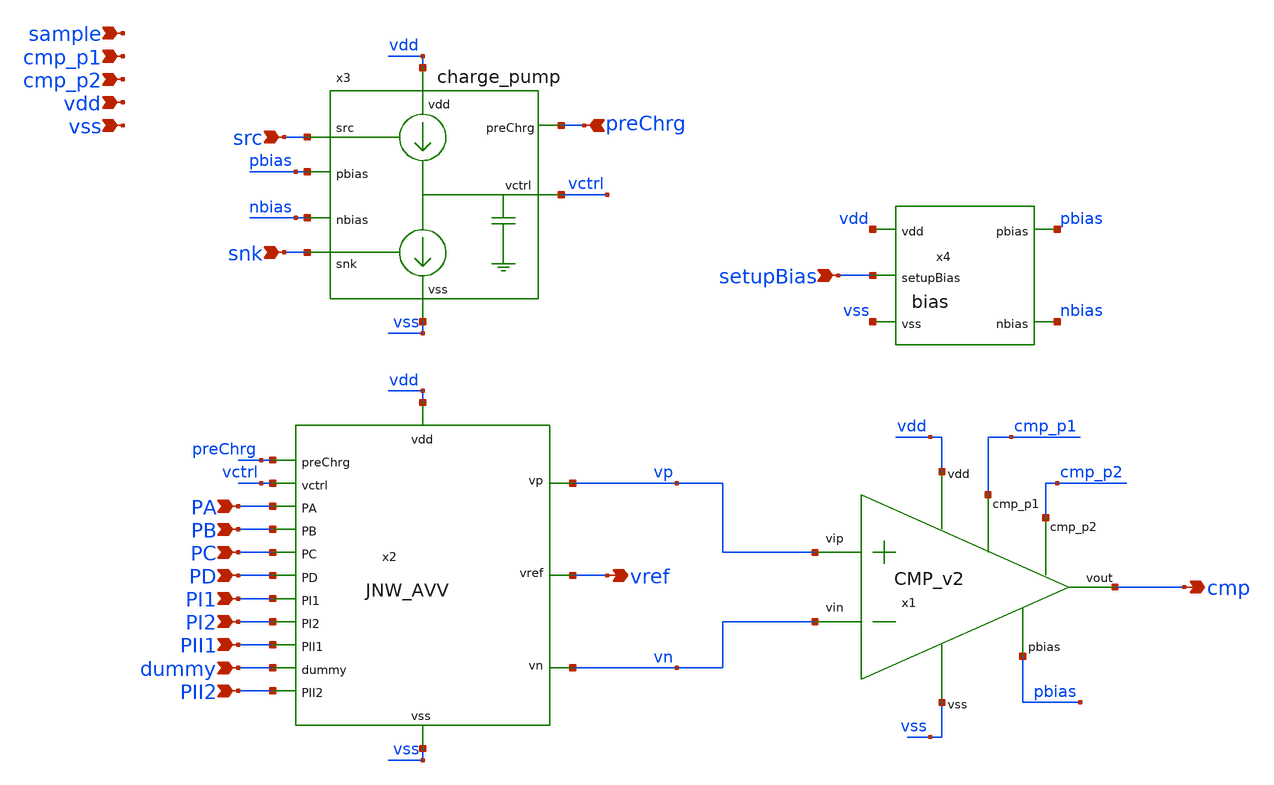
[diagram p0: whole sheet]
** sch_path: design/JNW_AVV_SKY130A/TB_bandgap.sch
**.subckt TB_bandgap vdd vss vref src snk PA PB PC PD PI1 PI2 PII1 cmp preChrg dummy PII2 setupBias
*+ cmp_p1 cmp_p2 sample
*.ipin vdd
*.ipin vss
*.opin vref
*.ipin src
*.ipin snk
*.ipin PA
*.ipin PB
*.ipin PC
*.ipin PD
*.ipin PI1
*.ipin PI2
*.ipin PII1
*.opin cmp
*.ipin preChrg
*.ipin dummy
*.ipin PII2
*.ipin setupBias
*.ipin cmp_p1
*.ipin cmp_p2
*.ipin sample
x2 vctrl PA PD vref vdd vss PC PB dummy PI2 PI1 PII1 vn vp PII2 preChrg JNW_AVV
x4 pbias vdd nbias vss setupBias bias
x1 vdd pbias cmp vn vp vss cmp_p1 cmp_p2 CMP_v2
x3 vdd pbias src vctrl snk nbias vss preChrg charge_pump
**.ends
.end
